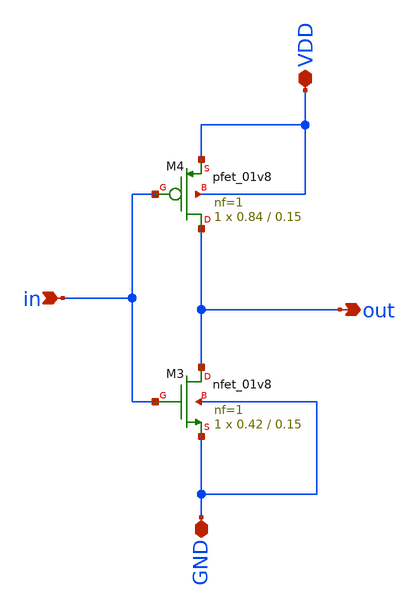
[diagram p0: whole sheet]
** sch_path: assignments/assignment6/inv.sch
**.subckt inv in GND VDD out
*.ipin in
*.iopin GND
*.iopin VDD
*.opin out
XM3 out in GND GND sky130_fd_pr__nfet_01v8 L=0.15 W=0.42 nf=1 ad='int((nf+1)/2) * W/nf * 0.29' as='int((nf+2)/2) * W/nf * 0.29'
+ pd='2*int((nf+1)/2) * (W/nf + 0.29)' ps='2*int((nf+2)/2) * (W/nf + 0.29)' nrd='0.29 / W' nrs='0.29 / W'
+ sa=0 sb=0 sd=0 mult=1 m=1
XM4 out in VDD VDD sky130_fd_pr__pfet_01v8 L=0.15 W=0.84 nf=1 ad='int((nf+1)/2) * W/nf * 0.29' as='int((nf+2)/2) * W/nf * 0.29'
+ pd='2*int((nf+1)/2) * (W/nf + 0.29)' ps='2*int((nf+2)/2) * (W/nf + 0.29)' nrd='0.29 / W' nrs='0.29 / W'
+ sa=0 sb=0 sd=0 mult=1 m=1
**.ends
.end
